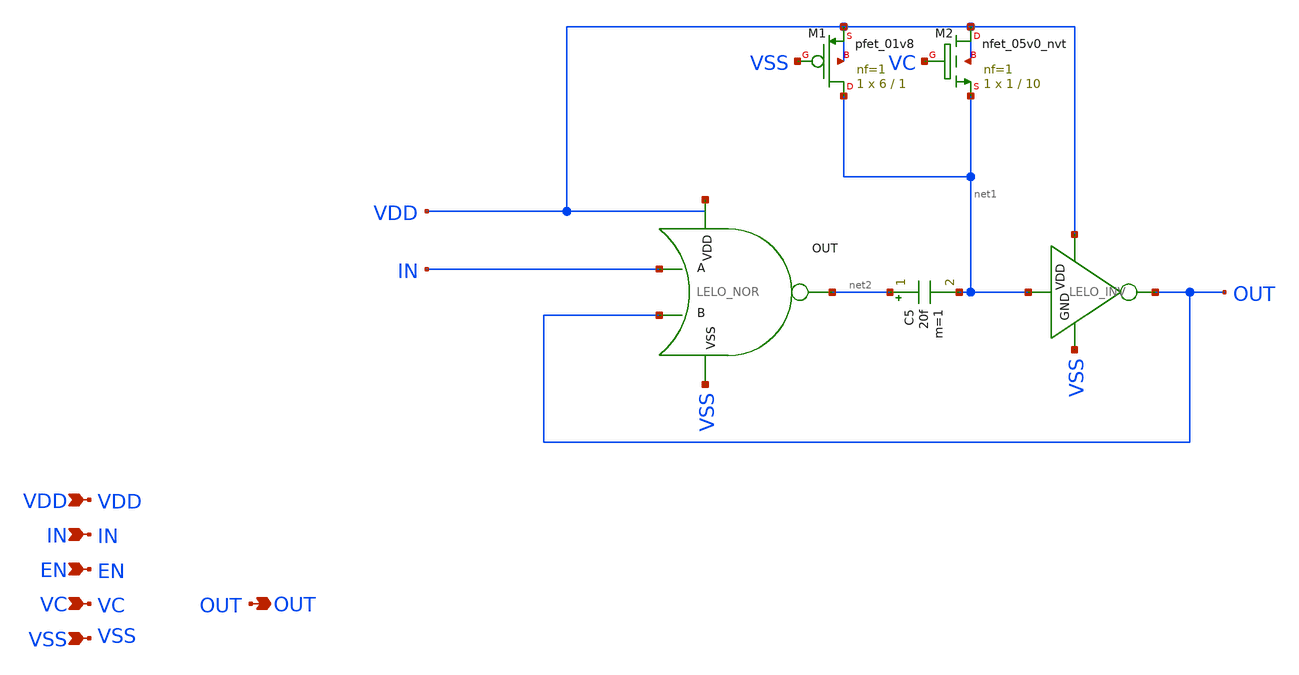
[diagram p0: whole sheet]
** sch_path: design/LELO_SVOD_SKY130A/LELO_ONESHOT_VC2.sch
**.subckt LELO_ONESHOT_VC2 VDD IN VC VSS OUT EN
*.ipin VDD
*.ipin IN
*.ipin VC
*.ipin VSS
*.opin OUT
*.ipin EN
x2 net3 net2 IN OUT VSS LELO_NOR
C5 net2 net1 20f m=1
x3 VDD net1 OUT VSS LELO_INV
XM1 net1 VSS VDD VDD sky130_fd_pr__pfet_01v8 L=1 W=6 nf=1 ad='int((1 + 1)/2) * 6 / 1 * 0.29' as='int((1 + 2)/2) * 6 / 1 * 0.29'
+ pd='2*int((1 + 1)/2) * (6 / 1 + 0.29)' ps='2*int((1 + 2)/2) * (6 / 1 + 0.29)' nrd='0.29 / 6 ' nrs='0.29 / 6 '
+ sa=0 sb=0 sd=0 mult=1 m=1
XM2 VDD VC net1 VDD sky130_fd_pr__nfet_05v0_nvt L=10 W=1 nf=1 ad='int((1 + 1)/2) * 1 / 1 * 0.29' as='int((1 + 2)/2) * 1 / 1 * 0.29'
+ pd='2*int((1 + 1)/2) * (1 / 1 + 0.29)' ps='2*int((1 + 2)/2) * (1 / 1 + 0.29)' nrd='0.29 / 1 ' nrs='0.29 / 1 '
+ sa=0 sb=0 sd=0 mult=1 m=1
**.ends

* expanding   symbol:  LELO_SVOD_SKY130A/LELO_NOR.sym # of pins=5
** sym_path: design/LELO_SVOD_SKY130A/LELO_NOR.sym
** sch_path: design/LELO_SVOD_SKY130A/LELO_NOR.sch
.subckt LELO_NOR VDD OUT A B VSS
*.ipin VDD
*.ipin VSS
*.opin OUT
*.ipin A
*.ipin B
XM2 OUT B VSS VSS sky130_fd_pr__nfet_01v8 L=0.15 W=2 nf=1 ad='int((1 + 1)/2) * 2 / 1 * 0.29' as='int((1 + 2)/2) * 2 / 1 * 0.29'
+ pd='2*int((1 + 1)/2) * (2 / 1 + 0.29)' ps='2*int((1 + 2)/2) * (2 / 1 + 0.29)' nrd='0.29 / 2 ' nrs='0.29 / 2 '
+ sa=0 sb=0 sd=0 mult=1 m=1
XM1 OUT A VSS VSS sky130_fd_pr__nfet_01v8 L=0.15 W=2 nf=1 ad='int((1 + 1)/2) * 2 / 1 * 0.29' as='int((1 + 2)/2) * 2 / 1 * 0.29'
+ pd='2*int((1 + 1)/2) * (2 / 1 + 0.29)' ps='2*int((1 + 2)/2) * (2 / 1 + 0.29)' nrd='0.29 / 2 ' nrs='0.29 / 2 '
+ sa=0 sb=0 sd=0 mult=1 m=1
XM3 OUT B net1 VDD sky130_fd_pr__pfet_01v8 L=0.15 W=4 nf=1 ad='int((1 + 1)/2) * 4 / 1 * 0.29' as='int((1 + 2)/2) * 4 / 1 * 0.29'
+ pd='2*int((1 + 1)/2) * (4 / 1 + 0.29)' ps='2*int((1 + 2)/2) * (4 / 1 + 0.29)' nrd='0.29 / 4 ' nrs='0.29 / 4 '
+ sa=0 sb=0 sd=0 mult=1 m=1
XM4 net1 A VDD VDD sky130_fd_pr__pfet_01v8 L=0.15 W=4 nf=1 ad='int((1 + 1)/2) * 4 / 1 * 0.29' as='int((1 + 2)/2) * 4 / 1 * 0.29'
+ pd='2*int((1 + 1)/2) * (4 / 1 + 0.29)' ps='2*int((1 + 2)/2) * (4 / 1 + 0.29)' nrd='0.29 / 4 ' nrs='0.29 / 4 '
+ sa=0 sb=0 sd=0 mult=1 m=1
.ends


* expanding   symbol:  LELO_SVOD_SKY130A/LELO_INV.sym # of pins=4
** sym_path: design/LELO_SVOD_SKY130A/LELO_INV.sym
** sch_path: design/LELO_SVOD_SKY130A/LELO_INV.sch
.subckt LELO_INV VDD VIN VOUT GND
*.ipin VIN
*.ipin VDD
*.ipin GND
*.opin VOUT
XM1 VOUT VIN GND GND sky130_fd_pr__nfet_01v8_lvt L=0.15 W=1 nf=1 ad='int((1 + 1)/2) * 1 / 1 * 0.29' as='int((1 + 2)/2) * 1 / 1 * 0.29'
+ pd='2*int((1 + 1)/2) * (1 / 1 + 0.29)' ps='2*int((1 + 2)/2) * (1 / 1 + 0.29)' nrd='0.29 / 1 ' nrs='0.29 / 1 '
+ sa=0 sb=0 sd=0 mult=1 m=1
XM2 VOUT VIN VDD VDD sky130_fd_pr__pfet_01v8_lvt L=0.35 W=1 nf=1 ad='int((1 + 1)/2) * 1 / 1 * 0.29' as='int((1 + 2)/2) * 1 / 1 * 0.29'
+ pd='2*int((1 + 1)/2) * (1 / 1 + 0.29)' ps='2*int((1 + 2)/2) * (1 / 1 + 0.29)' nrd='0.29 / 1 ' nrs='0.29 / 1 '
+ sa=0 sb=0 sd=0 mult=2 m=2
.ends

.end
